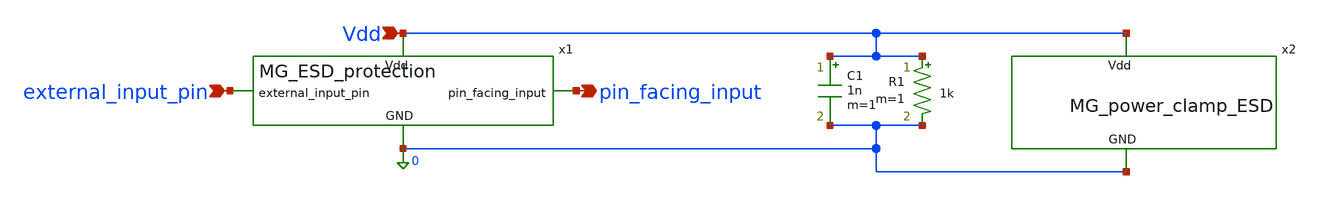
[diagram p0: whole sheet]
** sch_path: MG_ESD_protection/MG_ESD_protection_testbench.sch
**.subckt MG_ESD_protection_testbench external_input_pin Vdd pin_facing_input
*.ipin external_input_pin
*.ipin Vdd
*.opin pin_facing_input
x1 Vdd external_input_pin pin_facing_input 0 MG_ESD_protection
C1 Vdd 0 1n m=1
R1 Vdd 0 1k m=1
x2 Vdd 0 MG_power_clamp_ESD
**** begin user architecture code



.include /foss/pdks/gf180mcuD/libs.tech/ngspice/design.ngspice
.lib /foss/pdks/gf180mcuD/libs.tech/ngspice/sm141064.ngspice typical
.lib /foss/pdks/gf180mcuD/libs.tech/ngspice/sm141064.ngspice res_typical
.lib /foss/pdks/gf180mcuD/libs.tech/ngspice/sm141064.ngspice moscap_typical
.lib /foss/pdks/gf180mcuD/libs.tech/ngspice/sm141064.ngspice diode_typical
.lib /foss/pdks/gf180mcuD/libs.tech/ngspice/sm141064.ngspice mimcap_typical

* 1. Add ESD Current Source and Core Load Capacitor
* I_ESD injects the strike, and C_load represents the core receiver gate capacitance

I_ESD 0 external_input_pin PWL(0 0 1n 0)
C_load pin_facing_input 0 100f
Rleak Vdd 0 1G

.control

  * ==========================================
  * 3. HBM (Human Body Model) - 2kV Equivalent
  * Peak Current: ~1.33A, Rise: 5ns, Decay: ~150ns
  * ==========================================
  alter @I_ESD[pwl] = [ 0 0 5n 1.33 155n 0.49 305n 0.18 500n 0 ]

  * Run Transient Simulation (500ns duration, 1ns steps)
  tran 0.1n 500n

  * Extract Peak Voltages
  meas tran V_pad_max_HBM MAX v(external_input_pin)
  meas tran V_core_max_HBM MAX v(pin_facing_input)
  meas tran V_vdd_max_HBM MAX v(Vdd)

  * Print to Console
  print V_pad_max_HBM V_core_max_HBM


  * Plot HBM Waveforms
  plot v(external_input_pin) v(pin_facing_input) title 'HBM 2kV ESD Event' ylabel 'Voltage (V)' xlabel
+ 'Time (s)'
  plot v(pin_facing_input) title 'HBM 2kV ESD Event' ylabel 'Voltage (V)' xlabel 'Time (s)'


  * ==========================================
  * 4. CDM (Charged Device Model) - 500V Equivalent
  * Peak Current: ~5A, Rise: 250ps, Duration: ~2ns
  * ==========================================
  alter @I_ESD[pwl] = [ 0 0 250p 5.0 750p 0 1n -1.0 1.5n 0 3n 0 ]

  * Run Transient Simulation (3ns duration, 10ps steps)
  tran 5p 3n
  * Extract Peak Voltages
  meas tran V_pad_max_CDM MAX v(external_input_pin)
  meas tran V_core_max_CDM MAX v(pin_facing_input)
  meas tran V_vdd_max_CDM MAX v(Vdd)

  * Print to Console
  print V_pad_max_CDM V_core_max_CDM


  * Plot CDM Waveforms
  plot v(external_input_pin) v(pin_facing_input) title 'CDM 500V ESD Event' ylabel 'Voltage (V)' xlabel
+ 'Time (s)'
  plot v(pin_facing_input) title 'CDM 500V ESD Event' ylabel 'Voltage (V)' xlabel 'Time (s)'


.endc


**** end user architecture code
**.ends

* expanding   symbol:  MG_ESD_protection.sym # of pins=4
** sym_path: MG_ESD_protection/MG_ESD_protection.sym
** sch_path: MG_ESD_protection/MG_ESD_protection.sch
.subckt MG_ESD_protection Vdd external_input_pin pin_facing_input GND
*.ipin external_input_pin
*.ipin Vdd
*.ipin GND
*.opin pin_facing_input
D2 external_input_pin Vdd diode_pd2nw_06v0 area='25u * 0.9u ' pj='2*25u + 2*0.9u ' m=1
XR2 pin_facing_input external_input_pin GND ppolyf_u_1k_6p0 r_width=5e-6 r_length=10e-6 m=1
D1 GND external_input_pin diode_nd2ps_06v0 area='25u * 0.9u ' pj='2*25u + 2*0.9u ' m=1
D3 GND pin_facing_input diode_nd2ps_06v0 area='15u * 0.9u ' pj='2*15u + 2*0.9u ' m=1
D4 pin_facing_input Vdd diode_pd2nw_06v0 area='15u * 0.9u ' pj='2*15u + 2*0.9u ' m=1
D5 external_input_pin Vdd diode_pd2nw_06v0 area='25u * 0.9u ' pj='2*25u + 2*0.9u ' m=1
D6 GND external_input_pin diode_nd2ps_06v0 area='25u * 0.9u ' pj='2*25u + 2*0.9u ' m=1
D11 external_input_pin Vdd diode_pd2nw_06v0 area='25u * 0.9u ' pj='2*25u + 2*0.9u ' m=1
D12 GND external_input_pin diode_nd2ps_06v0 area='25u * 0.9u ' pj='2*25u + 2*0.9u ' m=1
D13 external_input_pin Vdd diode_pd2nw_06v0 area='25u * 0.9u ' pj='2*25u + 2*0.9u ' m=1
D14 GND external_input_pin diode_nd2ps_06v0 area='25u * 0.9u ' pj='2*25u + 2*0.9u ' m=1
D7 external_input_pin Vdd diode_pd2nw_06v0 area='25u * 0.9u ' pj='2*25u + 2*0.9u ' m=1
D8 GND external_input_pin diode_nd2ps_06v0 area='25u * 0.9u ' pj='2*25u + 2*0.9u ' m=1
D9 external_input_pin Vdd diode_pd2nw_06v0 area='25u * 0.9u ' pj='2*25u + 2*0.9u ' m=1
D10 GND external_input_pin diode_nd2ps_06v0 area='25u * 0.9u ' pj='2*25u + 2*0.9u ' m=1
.ends


* expanding   symbol:  MG_power_clamp_ESD.sym # of pins=2
** sym_path: MG_ESD_protection/MG_power_clamp_ESD.sym
** sch_path: MG_ESD_protection/MG_power_clamp_ESD.sch
.subckt MG_power_clamp_ESD Vdd GND
*.ipin Vdd
*.ipin GND
XMM_p1 clamp net1 Vdd Vdd pfet_05v0 L=0.9u W=12u nf=6 ad='int((nf+1)/2) * W/nf * 0.18u' as='int((nf+2)/2) * W/nf * 0.18u'
+ pd='2*int((nf+1)/2) * (W/nf + 0.18u)' ps='2*int((nf+2)/2) * (W/nf + 0.18u)' nrd='0.18u / W' nrs='0.18u / W'
+ sa=0 sb=0 sd=0 m=1
XMM_n1 clamp net1 GND GND nfet_05v0 L=0.9u W=4.8u nf=2 ad='int((nf+1)/2) * W/nf * 0.18u' as='int((nf+2)/2) * W/nf * 0.18u'
+ pd='2*int((nf+1)/2) * (W/nf + 0.18u)' ps='2*int((nf+2)/2) * (W/nf + 0.18u)' nrd='0.18u / W' nrs='0.18u / W'
+ sa=0 sb=0 sd=0 m=1
XC1 net1 GND cap_nmos_06v0 c_width=20e-6 c_length=20e-6 m=1
XMM_clamp3 Vdd clamp GND GND nfet_05v0 L=0.9u W=25u nf=1 ad='int((nf+1)/2) * W/nf * 0.18u' as='int((nf+2)/2) * W/nf * 0.18u'
+ pd='2*int((nf+1)/2) * (W/nf + 0.18u)' ps='2*int((nf+2)/2) * (W/nf + 0.18u)' nrd='0.18u / W' nrs='0.18u / W'
+ sa=0 sb=0 sd=0 m=1
XR2 net2 net3 GND ppolyf_u_1k_6p0 r_width=1e-6 r_length=4e-5 m=1
XR1 net3 net1 GND ppolyf_u_1k_6p0 r_width=1e-6 r_length=4e-5 m=1
XR3 net4 net5 GND ppolyf_u_1k_6p0 r_width=1e-6 r_length=4e-5 m=1
XR4 net5 net2 GND ppolyf_u_1k_6p0 r_width=1e-6 r_length=4e-5 m=1
XR5 net6 net7 GND ppolyf_u_1k_6p0 r_width=1e-6 r_length=4e-5 m=1
XR6 net7 net4 GND ppolyf_u_1k_6p0 r_width=1e-6 r_length=4e-5 m=1
XR7 Vdd net8 GND ppolyf_u_1k_6p0 r_width=1e-6 r_length=4e-5 m=1
XR8 net8 net6 GND ppolyf_u_1k_6p0 r_width=1e-6 r_length=4e-5 m=1
XMM_clamp1 Vdd clamp GND GND nfet_05v0 L=0.9u W=25u nf=1 ad='int((nf+1)/2) * W/nf * 0.18u' as='int((nf+2)/2) * W/nf * 0.18u'
+ pd='2*int((nf+1)/2) * (W/nf + 0.18u)' ps='2*int((nf+2)/2) * (W/nf + 0.18u)' nrd='0.18u / W' nrs='0.18u / W'
+ sa=0 sb=0 sd=0 m=1
XMM_clamp2 Vdd clamp GND GND nfet_05v0 L=0.9u W=25u nf=1 ad='int((nf+1)/2) * W/nf * 0.18u' as='int((nf+2)/2) * W/nf * 0.18u'
+ pd='2*int((nf+1)/2) * (W/nf + 0.18u)' ps='2*int((nf+2)/2) * (W/nf + 0.18u)' nrd='0.18u / W' nrs='0.18u / W'
+ sa=0 sb=0 sd=0 m=1
XMM_clamp4 Vdd clamp GND GND nfet_05v0 L=0.9u W=25u nf=1 ad='int((nf+1)/2) * W/nf * 0.18u' as='int((nf+2)/2) * W/nf * 0.18u'
+ pd='2*int((nf+1)/2) * (W/nf + 0.18u)' ps='2*int((nf+2)/2) * (W/nf + 0.18u)' nrd='0.18u / W' nrs='0.18u / W'
+ sa=0 sb=0 sd=0 m=1
XMM_clamp5 Vdd clamp GND GND nfet_05v0 L=0.9u W=25u nf=1 ad='int((nf+1)/2) * W/nf * 0.18u' as='int((nf+2)/2) * W/nf * 0.18u'
+ pd='2*int((nf+1)/2) * (W/nf + 0.18u)' ps='2*int((nf+2)/2) * (W/nf + 0.18u)' nrd='0.18u / W' nrs='0.18u / W'
+ sa=0 sb=0 sd=0 m=1
XMM_clamp6 Vdd clamp GND GND nfet_05v0 L=0.9u W=25u nf=1 ad='int((nf+1)/2) * W/nf * 0.18u' as='int((nf+2)/2) * W/nf * 0.18u'
+ pd='2*int((nf+1)/2) * (W/nf + 0.18u)' ps='2*int((nf+2)/2) * (W/nf + 0.18u)' nrd='0.18u / W' nrs='0.18u / W'
+ sa=0 sb=0 sd=0 m=1
XMM_clamp7 Vdd clamp GND GND nfet_05v0 L=0.9u W=25u nf=1 ad='int((nf+1)/2) * W/nf * 0.18u' as='int((nf+2)/2) * W/nf * 0.18u'
+ pd='2*int((nf+1)/2) * (W/nf + 0.18u)' ps='2*int((nf+2)/2) * (W/nf + 0.18u)' nrd='0.18u / W' nrs='0.18u / W'
+ sa=0 sb=0 sd=0 m=1
XMM_clamp8 Vdd clamp GND GND nfet_05v0 L=0.9u W=25u nf=1 ad='int((nf+1)/2) * W/nf * 0.18u' as='int((nf+2)/2) * W/nf * 0.18u'
+ pd='2*int((nf+1)/2) * (W/nf + 0.18u)' ps='2*int((nf+2)/2) * (W/nf + 0.18u)' nrd='0.18u / W' nrs='0.18u / W'
+ sa=0 sb=0 sd=0 m=1
XMM_clamp9 Vdd clamp GND GND nfet_05v0 L=0.9u W=25u nf=1 ad='int((nf+1)/2) * W/nf * 0.18u' as='int((nf+2)/2) * W/nf * 0.18u'
+ pd='2*int((nf+1)/2) * (W/nf + 0.18u)' ps='2*int((nf+2)/2) * (W/nf + 0.18u)' nrd='0.18u / W' nrs='0.18u / W'
+ sa=0 sb=0 sd=0 m=1
XMM_clamp10 Vdd clamp GND GND nfet_05v0 L=0.9u W=25u nf=1 ad='int((nf+1)/2) * W/nf * 0.18u' as='int((nf+2)/2) * W/nf * 0.18u'
+ pd='2*int((nf+1)/2) * (W/nf + 0.18u)' ps='2*int((nf+2)/2) * (W/nf + 0.18u)' nrd='0.18u / W' nrs='0.18u / W'
+ sa=0 sb=0 sd=0 m=1
XMM_clamp11 Vdd clamp GND GND nfet_05v0 L=0.9u W=25u nf=1 ad='int((nf+1)/2) * W/nf * 0.18u' as='int((nf+2)/2) * W/nf * 0.18u'
+ pd='2*int((nf+1)/2) * (W/nf + 0.18u)' ps='2*int((nf+2)/2) * (W/nf + 0.18u)' nrd='0.18u / W' nrs='0.18u / W'
+ sa=0 sb=0 sd=0 m=1
XMM_clamp12 Vdd clamp GND GND nfet_05v0 L=0.9u W=25u nf=1 ad='int((nf+1)/2) * W/nf * 0.18u' as='int((nf+2)/2) * W/nf * 0.18u'
+ pd='2*int((nf+1)/2) * (W/nf + 0.18u)' ps='2*int((nf+2)/2) * (W/nf + 0.18u)' nrd='0.18u / W' nrs='0.18u / W'
+ sa=0 sb=0 sd=0 m=1
.ends

.end
